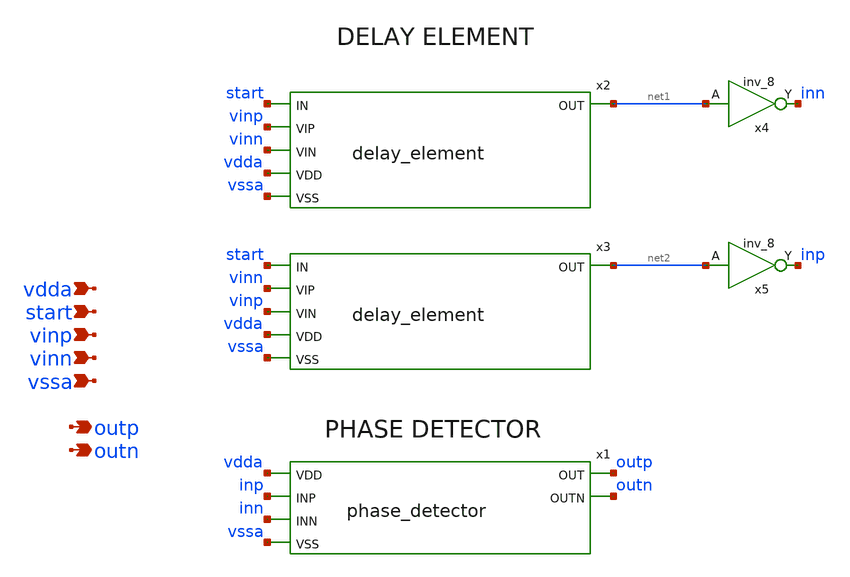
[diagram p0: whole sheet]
** sch_path: xschem/tdc.sch
**.subckt tdc vinn vinp vdda vssa start outp outn
*.ipin vinn
*.ipin vinp
*.ipin vdda
*.ipin vssa
*.ipin start
*.opin outp
*.opin outn
x1 vdda inp inn vssa outp outn phase_detector
x4 net1 vssa vssa vdda vdda inn sky130_fd_sc_hd__inv_8
x5 net2 vssa vssa vdda vdda inp sky130_fd_sc_hd__inv_8
x2 start net1 vinp vinn vdda vssa delay_element
x3 start net2 vinn vinp vdda vssa delay_element
**** begin user architecture code

** opencircuitdesign pdks install
* .lib $::SKYWATER_MODELS/sky130.lib.spice tt
.include /usr/local/share/pdk/sky130A/libs.ref/sky130_fd_sc_hd/spice/sky130_fd_sc_hd.spice

**** end user architecture code
**.ends
.end
